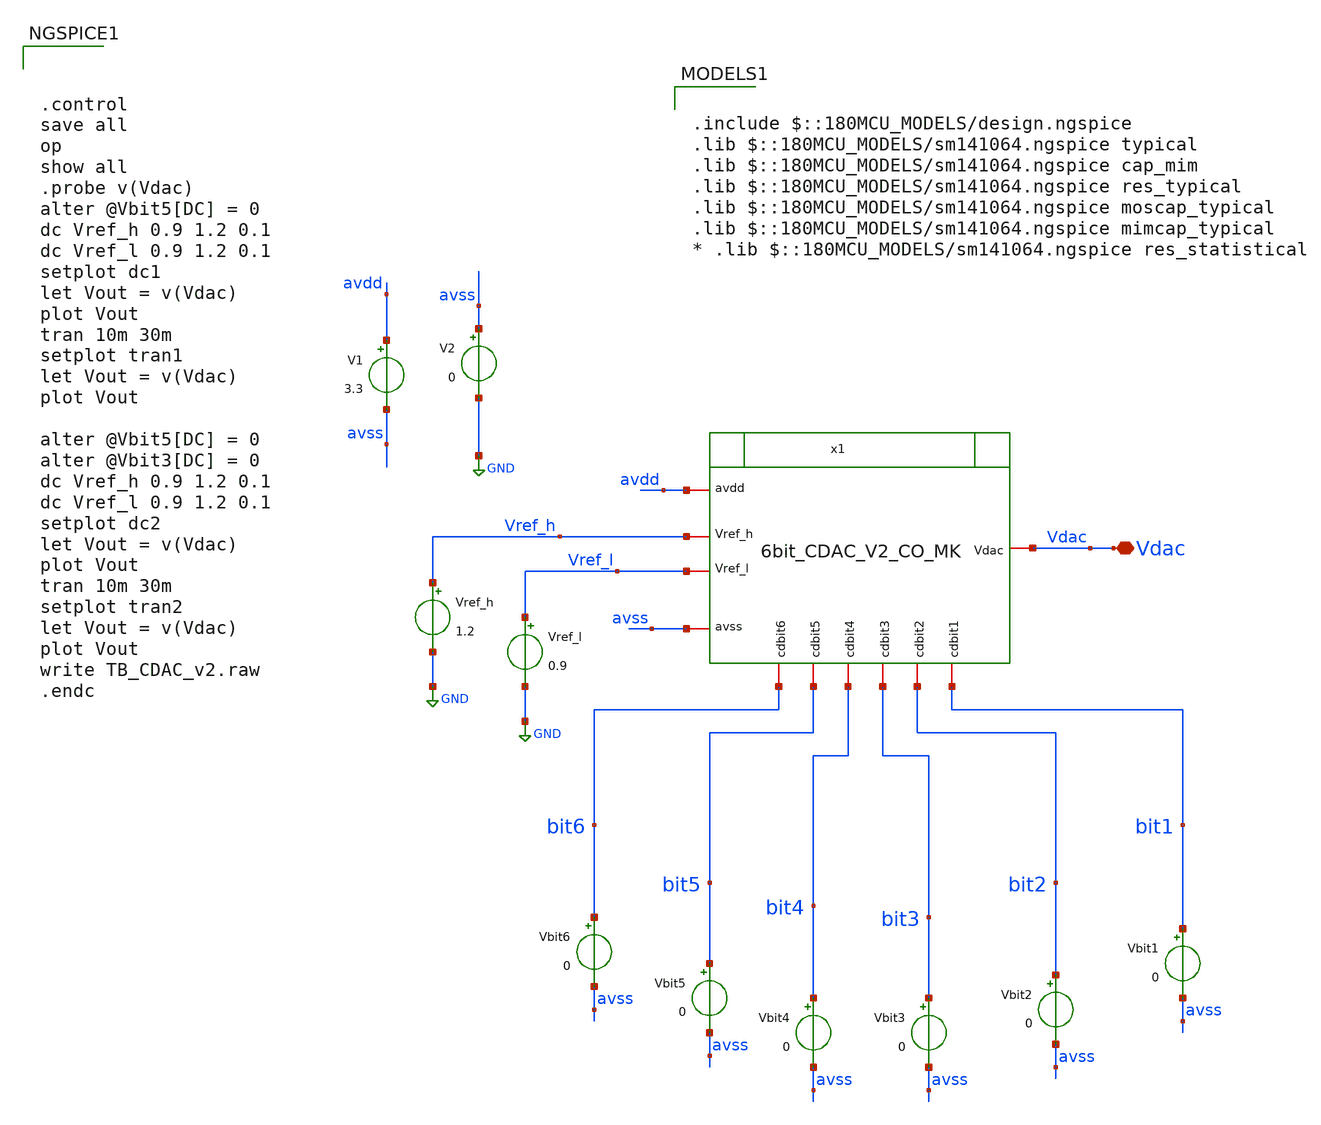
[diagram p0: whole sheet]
** sch_path: designs/libs/WK_Kadam/TB_6bit_CDAC_CO_V1_MK.sch
**.subckt TB_6bit_CDAC_CO_V1_MK Vdac
*.iopin Vdac
V1 avdd avss 3.3
V2 avss GND 0
Vbit1 bit1 avss 0
Vbit2 bit2 avss 0
Vbit3 bit3 avss 0
Vbit4 bit4 avss 0
Vbit5 bit5 avss 0
Vbit6 bit6 avss 0
Vref_h Vref_h GND 1.2
Vref_l Vref_l GND 0.9
**** begin user architecture code



.control
save all
op
show all
.probe v(Vdac)
alter @Vbit5[DC] = 0
dc Vref_h 0.9 1.2 0.1
dc Vref_l 0.9 1.2 0.1
setplot dc1
let Vout = v(Vdac)
plot Vout
tran 10m 30m
setplot tran1
let Vout = v(Vdac)
plot Vout

alter @Vbit5[DC] = 0
alter @Vbit3[DC] = 0
dc Vref_h 0.9 1.2 0.1
dc Vref_l 0.9 1.2 0.1
setplot dc2
let Vout = v(Vdac)
plot Vout
tran 10m 30m
setplot tran2
let Vout = v(Vdac)
plot Vout
write TB_CDAC_v2.raw
.endc



.include $::180MCU_MODELS/design.ngspice
.lib $::180MCU_MODELS/sm141064.ngspice typical
.lib $::180MCU_MODELS/sm141064.ngspice cap_mim
.lib $::180MCU_MODELS/sm141064.ngspice res_typical
.lib $::180MCU_MODELS/sm141064.ngspice moscap_typical
.lib $::180MCU_MODELS/sm141064.ngspice mimcap_typical
* .lib $::180MCU_MODELS/sm141064.ngspice res_statistical

**** end user architecture code
**.ends
.GLOBAL GND
.end
